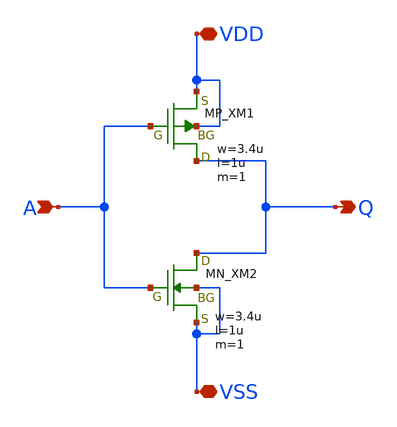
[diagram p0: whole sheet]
** sch_path: member_project/inverter_MUX/INV_01.sch
**.subckt INV_01 A VSS Q VDD
*.ipin A
*.iopin VSS
*.opin Q
*.iopin VDD
XM1 Q A VDD VDD PMOS w=3.4u l=1u as=0 ad=0 ps=0 pd=0 nrd=0 nrs=0 m=1
XM2 Q A VSS VSS NMOS w=3.4u l=1u as=0 ad=0 ps=0 pd=0 nrd=0 nrs=0 m=1
**.ends
.end
